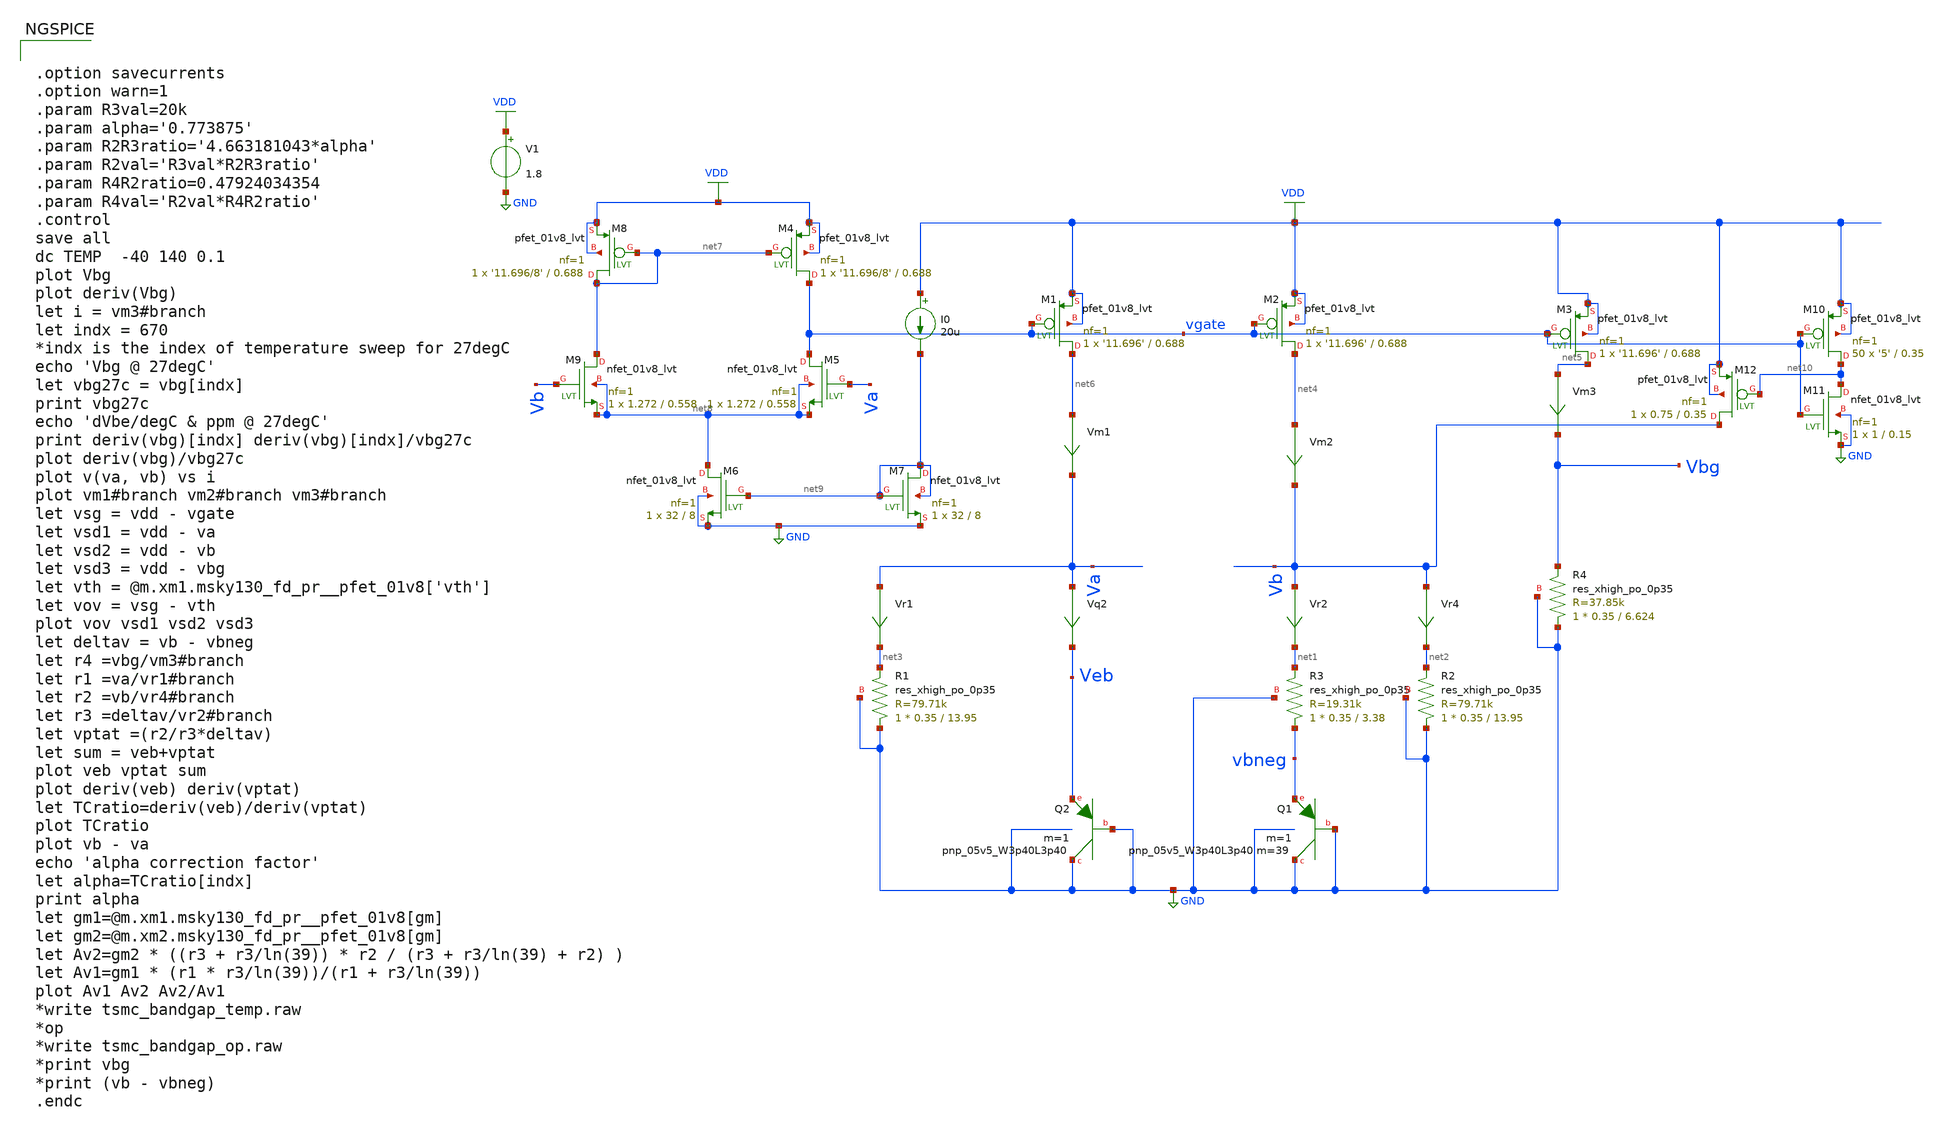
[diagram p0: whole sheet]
** sch_path: schematics/tsmc_bandgap_real_but_bias_current.sch
**.subckt tsmc_bandgap_real_but_bias_current
XQ2 GND GND Veb sky130_fd_pr__pnp_05v5_W3p40L3p40 m=1
V1 VDD GND 1.8
Vr4 Vb net2 0
.save i(vr4)
Vr2 Vb net1 0
.save i(vr2)
Vm1 net6 Va 0
.save i(vm1)
Vm2 net4 Vb 0
.save i(vm2)
Vm3 net5 Vbg 0
.save i(vm3)
Vr1 Va net3 0
.save i(vr1)
Vq2 Va Veb 0
.save i(vq2)
XQ1 GND GND vbneg sky130_fd_pr__pnp_05v5_W3p40L3p40 m=39 m=1
XR1 GND net3 GND sky130_fd_pr__res_xhigh_po_0p35 L=13.95 mult=1 m=1
XR3 vbneg net1 GND sky130_fd_pr__res_xhigh_po_0p35 L=3.38 mult=1 m=1
XR4 GND Vbg GND sky130_fd_pr__res_xhigh_po_0p35 L=6.624 mult=1 m=1
XR2 GND net2 GND sky130_fd_pr__res_xhigh_po_0p35 L=13.95 mult=1 m=1
XM4 vgate net7 VDD VDD sky130_fd_pr__pfet_01v8_lvt L=0.688 W='11.696/8' nf=1 ad='int((nf+1)/2) * W/nf * 0.29'
+ as='int((nf+2)/2) * W/nf * 0.29' pd='2*int((nf+1)/2) * (W/nf + 0.29)' ps='2*int((nf+2)/2) * (W/nf + 0.29)'
+ nrd='0.29 / W' nrs='0.29 / W' sa=0 sb=0 sd=0 mult=1 m=1
XM5 vgate Va net8 net8 sky130_fd_pr__nfet_01v8_lvt L=0.558 W=1.272 nf=1 ad='int((nf+1)/2) * W/nf * 0.29'
+ as='int((nf+2)/2) * W/nf * 0.29' pd='2*int((nf+1)/2) * (W/nf + 0.29)' ps='2*int((nf+2)/2) * (W/nf + 0.29)'
+ nrd='0.29 / W' nrs='0.29 / W' sa=0 sb=0 sd=0 mult=1 m=1
XM6 net8 net9 GND GND sky130_fd_pr__nfet_01v8_lvt L=8 W=32 nf=1 ad='int((nf+1)/2) * W/nf * 0.29' as='int((nf+2)/2) * W/nf * 0.29'
+ pd='2*int((nf+1)/2) * (W/nf + 0.29)' ps='2*int((nf+2)/2) * (W/nf + 0.29)' nrd='0.29 / W' nrs='0.29 / W'
+ sa=0 sb=0 sd=0 mult=1 m=1
XM8 net7 net7 VDD VDD sky130_fd_pr__pfet_01v8_lvt L=0.688 W='11.696/8' nf=1 ad='int((nf+1)/2) * W/nf * 0.29'
+ as='int((nf+2)/2) * W/nf * 0.29' pd='2*int((nf+1)/2) * (W/nf + 0.29)' ps='2*int((nf+2)/2) * (W/nf + 0.29)'
+ nrd='0.29 / W' nrs='0.29 / W' sa=0 sb=0 sd=0 mult=1 m=1
XM9 net7 Vb net8 net8 sky130_fd_pr__nfet_01v8_lvt L=0.558 W=1.272 nf=1 ad='int((nf+1)/2) * W/nf * 0.29'
+ as='int((nf+2)/2) * W/nf * 0.29' pd='2*int((nf+1)/2) * (W/nf + 0.29)' ps='2*int((nf+2)/2) * (W/nf + 0.29)'
+ nrd='0.29 / W' nrs='0.29 / W' sa=0 sb=0 sd=0 mult=1 m=1
I0 VDD net9 20u
XM1 net6 vgate VDD VDD sky130_fd_pr__pfet_01v8_lvt L=0.688 W='11.696' nf=1 ad='int((nf+1)/2) * W/nf * 0.29'
+ as='int((nf+2)/2) * W/nf * 0.29' pd='2*int((nf+1)/2) * (W/nf + 0.29)' ps='2*int((nf+2)/2) * (W/nf + 0.29)'
+ nrd='0.29 / W' nrs='0.29 / W' sa=0 sb=0 sd=0 mult=1 m=1
XM7 net9 net9 GND net9 sky130_fd_pr__nfet_01v8_lvt L=8 W=32 nf=1 ad='int((nf+1)/2) * W/nf * 0.29' as='int((nf+2)/2) * W/nf * 0.29'
+ pd='2*int((nf+1)/2) * (W/nf + 0.29)' ps='2*int((nf+2)/2) * (W/nf + 0.29)' nrd='0.29 / W' nrs='0.29 / W'
+ sa=0 sb=0 sd=0 mult=1 m=1
XM2 net4 vgate VDD VDD sky130_fd_pr__pfet_01v8_lvt L=0.688 W='11.696' nf=1 ad='int((nf+1)/2) * W/nf * 0.29'
+ as='int((nf+2)/2) * W/nf * 0.29' pd='2*int((nf+1)/2) * (W/nf + 0.29)' ps='2*int((nf+2)/2) * (W/nf + 0.29)'
+ nrd='0.29 / W' nrs='0.29 / W' sa=0 sb=0 sd=0 mult=1 m=1
XM3 net5 vgate VDD VDD sky130_fd_pr__pfet_01v8_lvt L=0.688 W='11.696' nf=1 ad='int((nf+1)/2) * W/nf * 0.29'
+ as='int((nf+2)/2) * W/nf * 0.29' pd='2*int((nf+1)/2) * (W/nf + 0.29)' ps='2*int((nf+2)/2) * (W/nf + 0.29)'
+ nrd='0.29 / W' nrs='0.29 / W' sa=0 sb=0 sd=0 mult=1 m=1
XM10 net10 vgate VDD VDD sky130_fd_pr__pfet_01v8_lvt L=0.35 W='5' nf=1 ad='int((nf+1)/2) * W/nf * 0.29'
+ as='int((nf+2)/2) * W/nf * 0.29' pd='2*int((nf+1)/2) * (W/nf + 0.29)' ps='2*int((nf+2)/2) * (W/nf + 0.29)'
+ nrd='0.29 / W' nrs='0.29 / W' sa=0 sb=0 sd=0 mult=50 m=50
XM11 net10 vgate GND GND sky130_fd_pr__nfet_01v8_lvt L=0.15 W=1 nf=1 ad='int((nf+1)/2) * W/nf * 0.29'
+ as='int((nf+2)/2) * W/nf * 0.29' pd='2*int((nf+1)/2) * (W/nf + 0.29)' ps='2*int((nf+2)/2) * (W/nf + 0.29)'
+ nrd='0.29 / W' nrs='0.29 / W' sa=0 sb=0 sd=0 mult=1 m=1
XM12 Vb net10 VDD VDD sky130_fd_pr__pfet_01v8_lvt L=0.35 W=0.75 nf=1 ad='int((nf+1)/2) * W/nf * 0.29'
+ as='int((nf+2)/2) * W/nf * 0.29' pd='2*int((nf+1)/2) * (W/nf + 0.29)' ps='2*int((nf+2)/2) * (W/nf + 0.29)'
+ nrd='0.29 / W' nrs='0.29 / W' sa=0 sb=0 sd=0 mult=1 m=1
**** begin user architecture code

.include $::SKYWATER_MODELS/cells/nfet_01v8/sky130_fd_pr__nfet_01v8__tt.corner.spice
.include $::SKYWATER_MODELS/cells/nfet_01v8_lvt/sky130_fd_pr__nfet_01v8_lvt__tt.corner.spice
.include $::SKYWATER_MODELS/cells/pfet_01v8/sky130_fd_pr__pfet_01v8__tt.corner.spice
.include $::SKYWATER_MODELS/cells/nfet_03v3_nvt/sky130_fd_pr__nfet_03v3_nvt__tt.corner.spice
.include $::SKYWATER_MODELS/cells/nfet_05v0_nvt/sky130_fd_pr__nfet_05v0_nvt__tt.corner.spice
.include $::SKYWATER_MODELS/cells/esd_nfet_01v8/sky130_fd_pr__esd_nfet_01v8__tt.corner.spice
.include $::SKYWATER_MODELS/cells/pfet_01v8_lvt/sky130_fd_pr__pfet_01v8_lvt__tt.corner.spice
.include $::SKYWATER_MODELS/cells/pfet_01v8_hvt/sky130_fd_pr__pfet_01v8_hvt__tt.corner.spice
.include $::SKYWATER_MODELS/cells/esd_pfet_g5v0d10v5/sky130_fd_pr__esd_pfet_g5v0d10v5__tt.corner.spice
.include $::SKYWATER_MODELS/cells/pfet_g5v0d10v5/sky130_fd_pr__pfet_g5v0d10v5__tt.corner.spice
.include $::SKYWATER_MODELS/cells/pfet_g5v0d16v0/sky130_fd_pr__pfet_g5v0d16v0__tt.corner.spice
.include $::SKYWATER_MODELS/cells/nfet_g5v0d10v5/sky130_fd_pr__nfet_g5v0d10v5__tt.corner.spice
.include $::SKYWATER_MODELS/cells/nfet_g5v0d16v0/sky130_fd_pr__nfet_g5v0d16v0__tt_discrete.corner.spice
.include $::SKYWATER_MODELS/cells/esd_nfet_g5v0d10v5/sky130_fd_pr__esd_nfet_g5v0d10v5__tt.corner.spice
.include $::SKYWATER_MODELS/models/corners/tt/nonfet.spice
* Mismatch parameters
.include $::SKYWATER_MODELS/cells/nfet_01v8/sky130_fd_pr__nfet_01v8__mismatch.corner.spice
.include $::SKYWATER_MODELS/cells/pfet_01v8/sky130_fd_pr__pfet_01v8__mismatch.corner.spice
.include $::SKYWATER_MODELS/cells/nfet_01v8_lvt/sky130_fd_pr__nfet_01v8_lvt__mismatch.corner.spice
.include $::SKYWATER_MODELS/cells/pfet_01v8_lvt/sky130_fd_pr__pfet_01v8_lvt__mismatch.corner.spice
.include $::SKYWATER_MODELS/cells/pfet_01v8_hvt/sky130_fd_pr__pfet_01v8_hvt__mismatch.corner.spice
.include $::SKYWATER_MODELS/cells/nfet_g5v0d10v5/sky130_fd_pr__nfet_g5v0d10v5__mismatch.corner.spice
.include $::SKYWATER_MODELS/cells/pfet_g5v0d10v5/sky130_fd_pr__pfet_g5v0d10v5__mismatch.corner.spice
.include $::SKYWATER_MODELS/cells/nfet_05v0_nvt/sky130_fd_pr__nfet_05v0_nvt__mismatch.corner.spice
.include $::SKYWATER_MODELS/cells/nfet_03v3_nvt/sky130_fd_pr__nfet_03v3_nvt__mismatch.corner.spice
* Resistor$::SKYWATER_MODELS/Capacitor
.include $::SKYWATER_MODELS/models/r+c/res_typical__cap_typical.spice
.include $::SKYWATER_MODELS/models/r+c/res_typical__cap_typical__lin.spice
* Special cells
.include $::SKYWATER_MODELS/models/corners/tt/specialized_cells.spice
* All models
.include $::SKYWATER_MODELS/models/all.spice
.include $::SKYWATER_MODELS/cells/pnp_05v5/sky130_fd_pr__pnp_05v5_W3p40L3p40.model.spice
* Corner
.include $::SKYWATER_MODELS/models/corners/tt/rf.spice



.option savecurrents
.option warn=1
.param R3val=20k
.param alpha='0.773875'
.param R2R3ratio='4.663181043*alpha'
.param R2val='R3val*R2R3ratio'
.param R4R2ratio=0.47924034354
.param R4val='R2val*R4R2ratio'
.control
save all
dc TEMP  -40 140 0.1
plot Vbg
plot deriv(Vbg)
let i = vm3#branch
let indx = 670
*indx is the index of temperature sweep for 27degC
echo 'Vbg @ 27degC'
let vbg27c = vbg[indx]
print vbg27c
echo 'dVbe/degC & ppm @ 27degC'
print deriv(vbg)[indx] deriv(vbg)[indx]/vbg27c
plot deriv(vbg)/vbg27c
plot v(va, vb) vs i
plot vm1#branch vm2#branch vm3#branch
let vsg = vdd - vgate
let vsd1 = vdd - va
let vsd2 = vdd - vb
let vsd3 = vdd - vbg
let vth = @m.xm1.msky130_fd_pr__pfet_01v8['vth']
let vov = vsg - vth
plot vov vsd1 vsd2 vsd3
let deltav = vb - vbneg
let r4 =vbg/vm3#branch
let r1 =va/vr1#branch
let r2 =vb/vr4#branch
let r3 =deltav/vr2#branch
let vptat =(r2/r3*deltav)
let sum = veb+vptat
plot veb vptat sum
plot deriv(veb) deriv(vptat)
let TCratio=deriv(veb)/deriv(vptat)
plot TCratio
plot vb - va
echo 'alpha correction factor'
let alpha=TCratio[indx]
print alpha
let gm1=@m.xm1.msky130_fd_pr__pfet_01v8[gm]
let gm2=@m.xm2.msky130_fd_pr__pfet_01v8[gm]
let Av2=gm2 * ((r3 + r3/ln(39)) * r2 / (r3 + r3/ln(39) + r2) )
let Av1=gm1 * (r1 * r3/ln(39))/(r1 + r3/ln(39))
plot Av1 Av2 Av2/Av1
*write tsmc_bandgap_temp.raw
*op
*write tsmc_bandgap_op.raw
*print vbg
*print (vb - vbneg)
.endc


**** end user architecture code
**.ends
.GLOBAL GND
.GLOBAL VDD
.end
